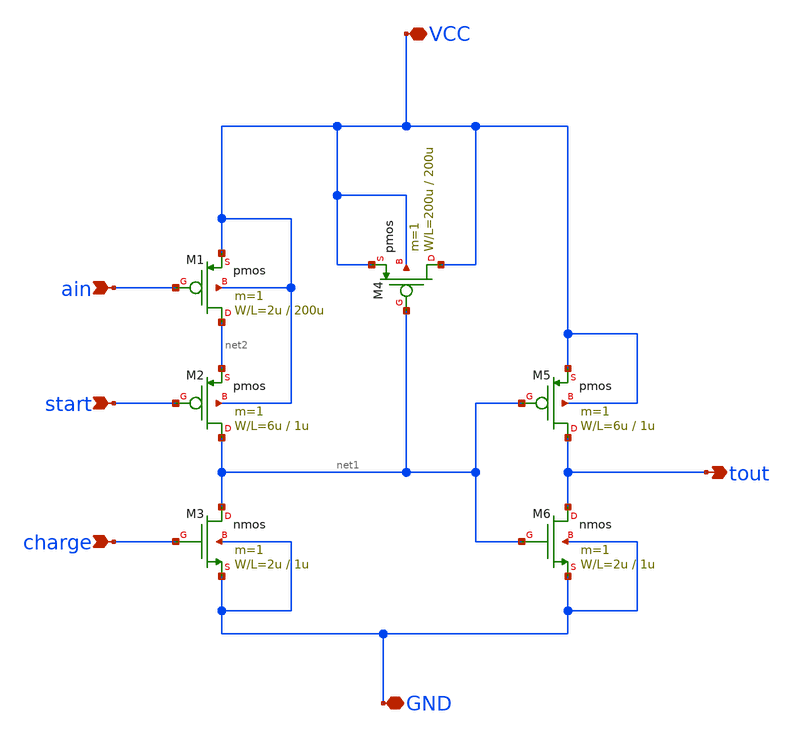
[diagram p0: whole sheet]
** sch_path: member_project/sanken/iijima/AnalogtoTime/AnalogtoTime.sch
**.subckt AnalogtoTime VCC ain tout GND start charge
*.iopin VCC
*.ipin ain
*.opin tout
*.iopin GND
*.ipin start
*.ipin charge
M1 net2 ain VCC VCC pmos L=200u W=2u m=1
M2 net1 start net2 VCC pmos L=1u W=6u m=1
M4 VCC net1 VCC VCC pmos L=200u W=200u m=1
M3 net1 charge GND GND nmos L=1u W=2u m=1
M6 tout net1 GND GND nmos L=1u W=2u m=1
M5 tout net1 VCC VCC pmos L=1u W=6u m=1
**.ends
.end
